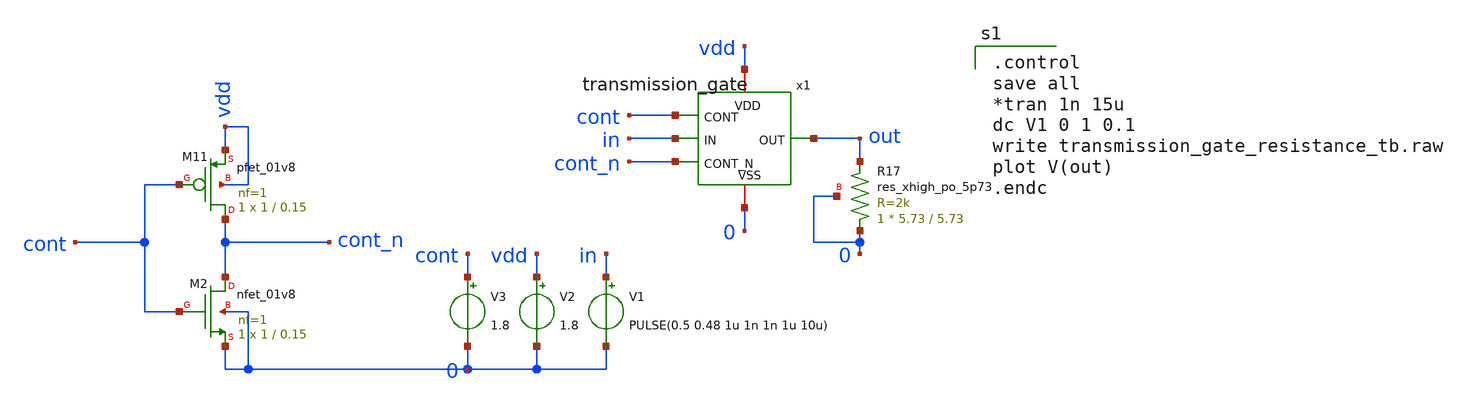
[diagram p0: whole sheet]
** sch_path: xschem/transmission_gate_resistance_tb.sch
**.subckt transmission_gate_resistance_tb
V1 in 0 PULSE(0.5 0.48 1u 1n 1n 1u 10u)
V2 vdd 0 1.8
V3 cont 0 1.8
x1 vdd out in cont 0 cont_n transmission_gate W=20 L=1 NF=1 M=1
XM2 cont_n cont 0 0 sky130_fd_pr__nfet_01v8 L=0.15 W=1 nf=1 ad='int((1 + 1)/2) * 1 / 1 * 0.29' as='int((1 + 2)/2) * 1 / 1 * 0.29'
+ pd='2*int((1 + 1)/2) * (1 / 1 + 0.29)' ps='2*int((1 + 2)/2) * (1 / 1 + 0.29)' nrd='0.29 / 1 ' nrs='0.29 / 1 '
+ sa=0 sb=0 sd=0 mult=1 m=1
XM11 cont_n cont vdd vdd sky130_fd_pr__pfet_01v8 L=0.15 W=1 nf=1 ad='int((nf+1)/2) * W/nf * 0.29' as='int((nf+2)/2) * W/nf * 0.29'
+ pd='2*int((nf+1)/2) * (W/nf + 0.29)' ps='2*int((nf+2)/2) * (W/nf + 0.29)' nrd='0.29 / W' nrs='0.29 / W'
+ sa=0 sb=0 sd=0 mult=1 m=1
XR17 0 out 0 sky130_fd_pr__res_xhigh_po_5p73 L=5.73 mult=1 m=1
**** begin user architecture code

.control
save all
*tran 1n 15u
dc V1 0 1 0.1
write transmission_gate_resistance_tb.raw
plot V(out)
.endc


** opencircuitdesign pdks install
.lib $::SKYWATER_MODELS/sky130.lib.spice tt


**** end user architecture code
**.ends

* expanding   symbol:  /foss/designs/Transmission-Gate/xschem/transmission_gate.sym # of pins=6
** sym_path: xschem/transmission_gate.sym
** sch_path: xschem/transmission_gate.sch
.subckt transmission_gate VDD OUT IN CONT VSS CONT_N  W=20 L=1 NF=1 M=1
*.opin OUT
*.ipin IN
*.iopin VDD
*.iopin VSS
*.ipin CONT
*.ipin CONT_N
XM2 IN CONT OUT VSS sky130_fd_pr__nfet_01v8 L=L W=W nf=NF ad='int((NF + 1)/2) * W / NF * 0.29' as='int((NF + 2)/2) * W / NF * 0.29'
+ pd='2*int((NF + 1)/2) * (W / NF + 0.29)' ps='2*int((NF + 2)/2) * (W / NF + 0.29)' nrd='0.29 / W ' nrs='0.29 / W '
+ sa=0 sb=0 sd=0 mult=M m=M
XM11 IN CONT_N OUT VDD sky130_fd_pr__pfet_01v8 L=L W=W nf=NF ad='int((nf+1)/2) * W/nf * 0.29' as='int((nf+2)/2) * W/nf * 0.29'
+ pd='2*int((nf+1)/2) * (W/nf + 0.29)' ps='2*int((nf+2)/2) * (W/nf + 0.29)' nrd='0.29 / W' nrs='0.29 / W'
+ sa=0 sb=0 sd=0 mult=M m=M
.ends

.end
